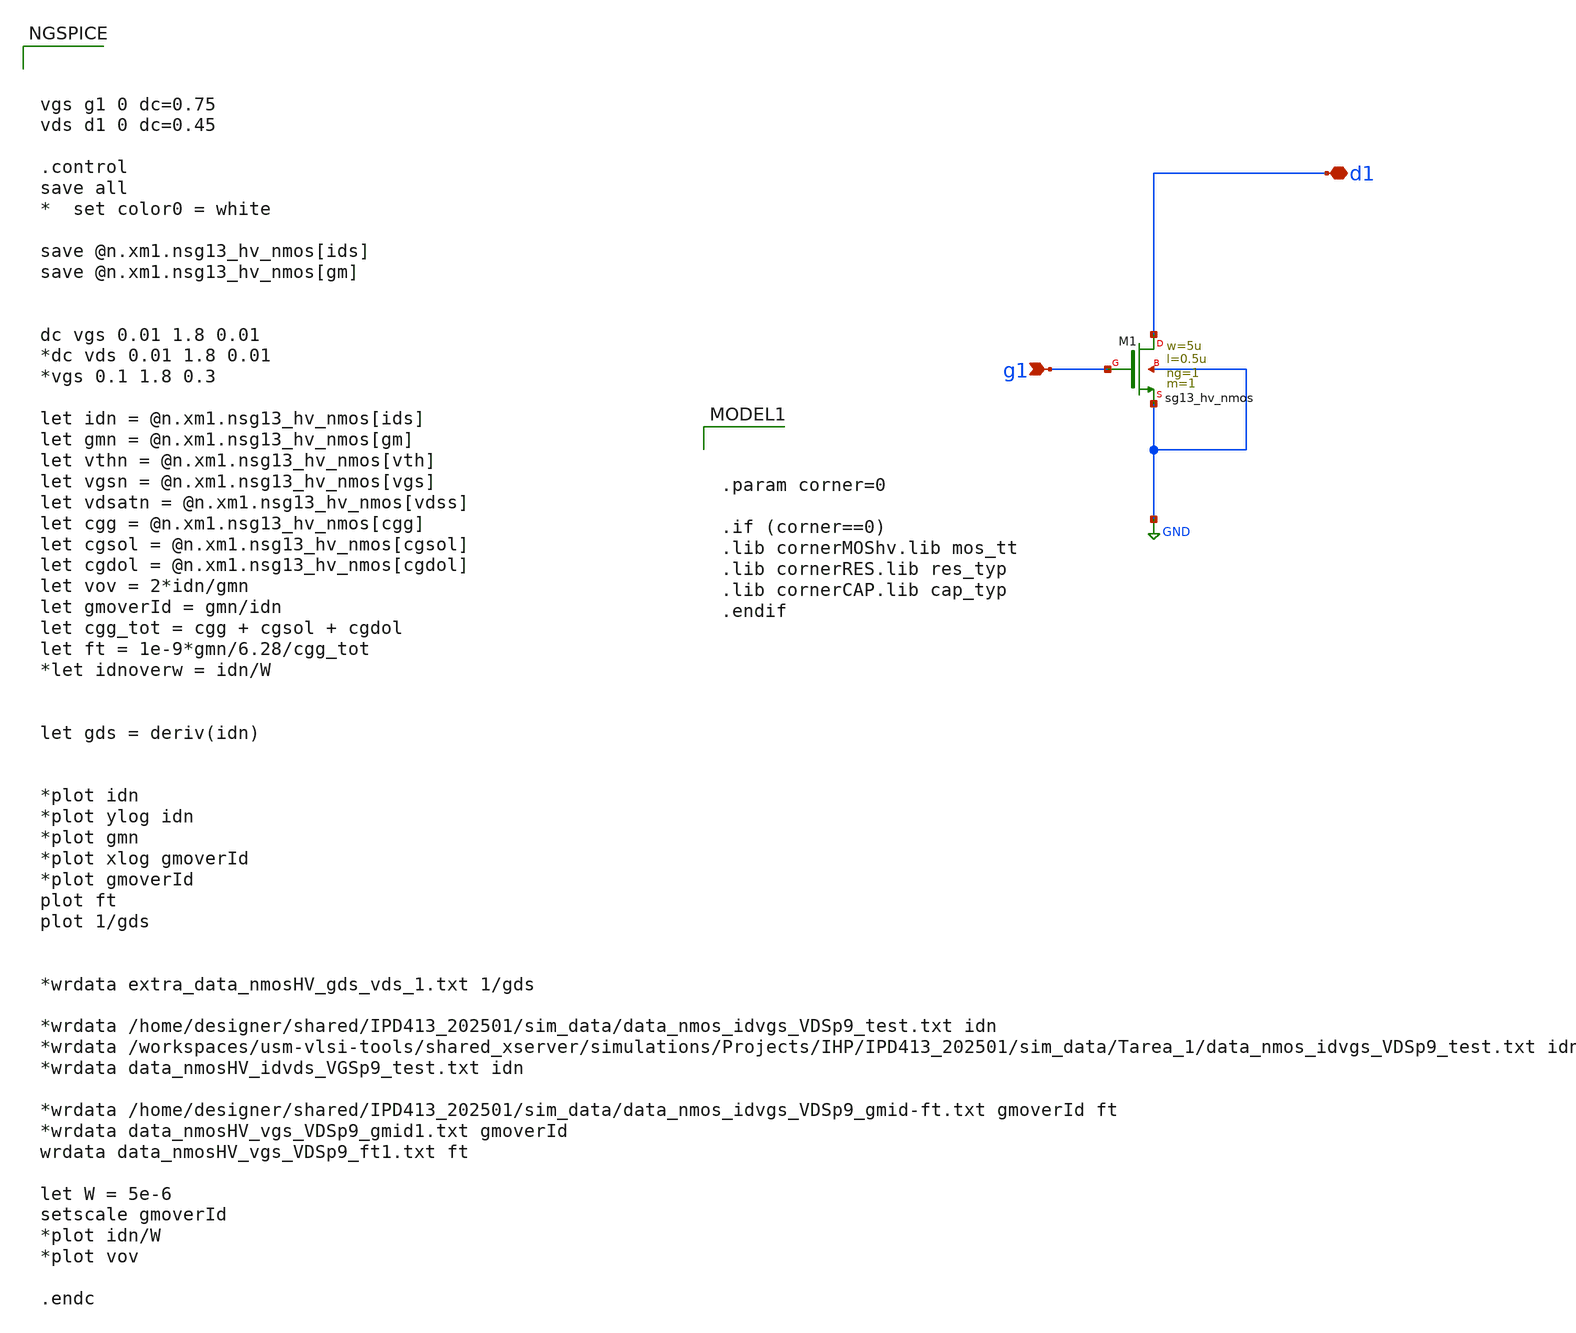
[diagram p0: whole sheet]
** sch_path: DelayLine/others/single mos/tb_nmosHv_charac.sch
**.subckt tb_nmosHv_charac g1 d1
*.ipin g1
*.iopin d1
XM1 d1 g1 GND GND sg13_hv_nmos w=5u l=0.5u ng=1 m=1 mm_ok=1
**** begin user architecture code



vgs g1 0 dc=0.75
vds d1 0 dc=0.45

.control
save all
*  set color0 = white

save @n.xm1.nsg13_hv_nmos[ids]
save @n.xm1.nsg13_hv_nmos[gm]


dc vgs 0.01 1.8 0.01
*dc vds 0.01 1.8 0.01
*vgs 0.1 1.8 0.3

let idn = @n.xm1.nsg13_hv_nmos[ids]
let gmn = @n.xm1.nsg13_hv_nmos[gm]
let vthn = @n.xm1.nsg13_hv_nmos[vth]
let vgsn = @n.xm1.nsg13_hv_nmos[vgs]
let vdsatn = @n.xm1.nsg13_hv_nmos[vdss]
let cgg = @n.xm1.nsg13_hv_nmos[cgg]
let cgsol = @n.xm1.nsg13_hv_nmos[cgsol]
let cgdol = @n.xm1.nsg13_hv_nmos[cgdol]
let vov = 2*idn/gmn
let gmoverId = gmn/idn
let cgg_tot = cgg + cgsol + cgdol
let ft = 1e-9*gmn/6.28/cgg_tot
*let idnoverw = idn/W


let gds = deriv(idn)


*plot idn
*plot ylog idn
*plot gmn
*plot xlog gmoverId
*plot gmoverId
plot ft
plot 1/gds


*wrdata extra_data_nmosHV_gds_vds_1.txt 1/gds

*wrdata /home/designer/shared/IPD413_202501/sim_data/data_nmos_idvgs_VDSp9_test.txt idn
*wrdata
*+ /workspaces/usm-vlsi-tools/shared_xserver/simulations/Projects/IHP/IPD413_202501/sim_data/Tarea_1/data_nmos_idvgs_VDSp9_test.txt idn
*wrdata data_nmosHV_idvds_VGSp9_test.txt idn

*wrdata /home/designer/shared/IPD413_202501/sim_data/data_nmos_idvgs_VDSp9_gmid-ft.txt gmoverId ft
*wrdata data_nmosHV_vgs_VDSp9_gmid1.txt gmoverId
wrdata data_nmosHV_vgs_VDSp9_ft1.txt ft

let W = 5e-6
setscale gmoverId
*plot idn/W
*plot vov

.endc




.param corner=0

.if (corner==0)
.lib cornerMOShv.lib mos_tt
.lib cornerRES.lib res_typ
.lib cornerCAP.lib cap_typ
.endif

**** end user architecture code
**.ends
.GLOBAL GND
.end
